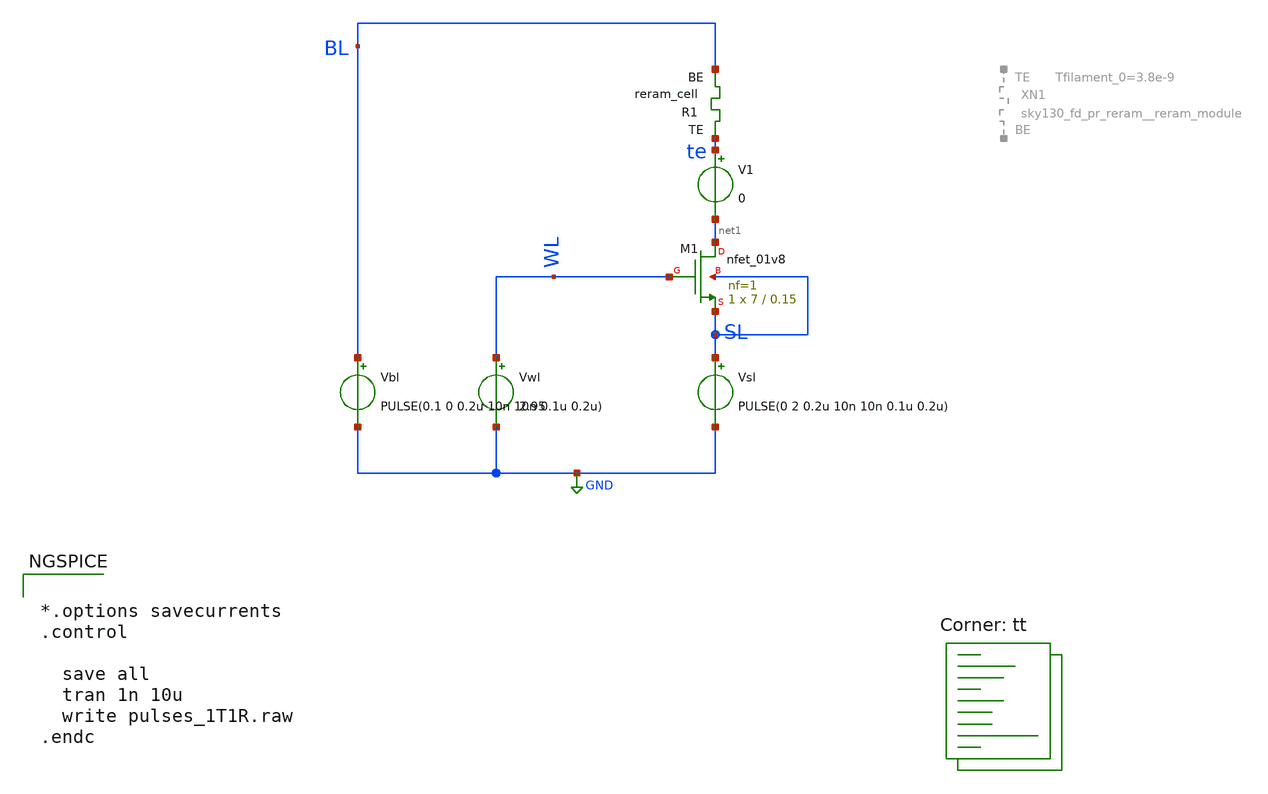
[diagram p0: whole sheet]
** sch_path: memristor_models/sky130_original/pulses_1T1R.sch
**.subckt pulses_1T1R
XM1 net1 WL SL SL sky130_fd_pr__nfet_01v8 L=0.15 W=7 nf=1 ad='int((nf+1)/2) * W/nf * 0.29' as='int((nf+2)/2) * W/nf * 0.29'
+ pd='2*int((nf+1)/2) * (W/nf + 0.29)' ps='2*int((nf+2)/2) * (W/nf + 0.29)' nrd='0.29 / W' nrs='0.29 / W'
+ sa=0 sb=0 sd=0 mult=1 m=1
Vwl WL GND 2.95
Vbl BL GND PULSE(0.1 0 0.2u 10n 10n 0.1u 0.2u)
V1 te net1 0
XR1 te BL sky130_fd_pr_reram__reram_cell Tfilament_0=3.3e-9
Vsl SL GND PULSE(0 2 0.2u 10n 10n 0.1u 0.2u)
**** begin user architecture code


*.options savecurrents
.control

  save all
  tran 1n 10u
  write pulses_1T1R.raw
.endc



.lib $::SKYWATER_MODELS/sky130.lib.spice tt

** opencircuitdesign pdks install
.inc $::SKYWATER_MODELS/sky130_fd_pr_reram__reram_cell.spice

**** end user architecture code
**.ends
.GLOBAL GND
.end
